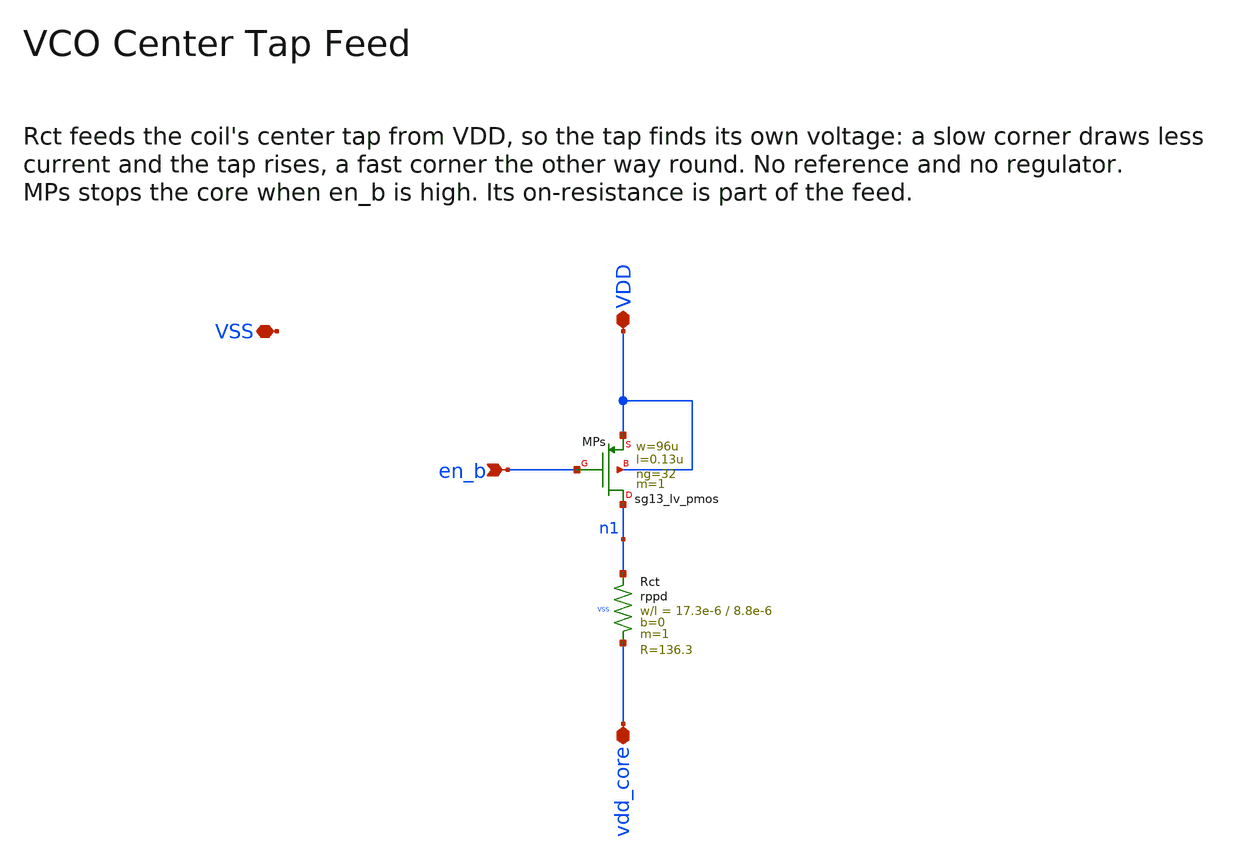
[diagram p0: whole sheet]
** sch_path: macros/vco/schematic/xschem/vco_feed.sch
**.subckt vco_feed VDD VSS en_b vdd_core
*.iopin VDD
*.iopin VSS
*.ipin en_b
*.iopin vdd_core
XMPs n1 en_b VDD VDD sg13_lv_pmos w=96u l=0.13u ng=32 m=1 mm_ok=1
XRct n1 vdd_core VSS rppd w=17.3e-6 l=8.8e-6 m=1 b=0 mm_ok=1
**.ends
.end
